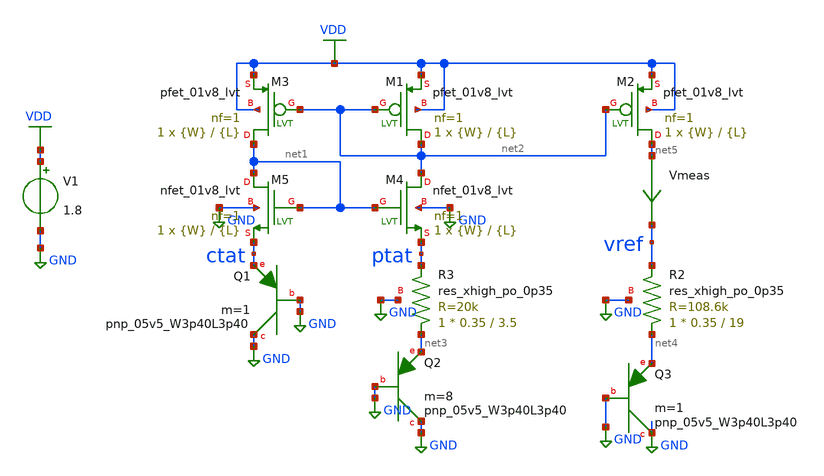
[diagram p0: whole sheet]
** sch_path: xschem/bgr.sch
**.subckt bgr
V1 VDD GND 1.8
XQ1 GND GND ctat sky130_fd_pr__pnp_05v5_W3p40L3p40 m=1
XQ2 GND GND net3 sky130_fd_pr__pnp_05v5_W3p40L3p40 m=8
XQ3 GND GND net4 sky130_fd_pr__pnp_05v5_W3p40L3p40 m=1
Vmeas net5 vref 0
.save i(vmeas)
XM3 net1 net2 VDD VDD sky130_fd_pr__pfet_01v8_lvt L={L} W={W} nf=1 ad='int((nf+1)/2) * W/nf * 0.29' as='int((nf+2)/2) * W/nf * 0.29'
+ pd='2*int((nf+1)/2) * (W/nf + 0.29)' ps='2*int((nf+2)/2) * (W/nf + 0.29)' nrd='0.29 / W' nrs='0.29 / W'
+ sa=0 sb=0 sd=0 mult=1 m=1
XM1 net2 net2 VDD VDD sky130_fd_pr__pfet_01v8_lvt L={L} W={W} nf=1 ad='int((nf+1)/2) * W/nf * 0.29' as='int((nf+2)/2) * W/nf * 0.29'
+ pd='2*int((nf+1)/2) * (W/nf + 0.29)' ps='2*int((nf+2)/2) * (W/nf + 0.29)' nrd='0.29 / W' nrs='0.29 / W'
+ sa=0 sb=0 sd=0 mult=1 m=1
XM2 net5 net2 VDD VDD sky130_fd_pr__pfet_01v8_lvt L={L} W={W} nf=1 ad='int((nf+1)/2) * W/nf * 0.29' as='int((nf+2)/2) * W/nf * 0.29'
+ pd='2*int((nf+1)/2) * (W/nf + 0.29)' ps='2*int((nf+2)/2) * (W/nf + 0.29)' nrd='0.29 / W' nrs='0.29 / W'
+ sa=0 sb=0 sd=0 mult=1 m=1
XM5 net1 net1 ctat GND sky130_fd_pr__nfet_01v8_lvt L={L} W={W} nf=1 ad='int((nf+1)/2) * W/nf * 0.29'
+ as='int((nf+2)/2) * W/nf * 0.29' pd='2*int((nf+1)/2) * (W/nf + 0.29)' ps='2*int((nf+2)/2) * (W/nf + 0.29)'
+ nrd='0.29 / W' nrs='0.29 / W' sa=0 sb=0 sd=0 mult=1 m=1
XM4 net2 net1 ptat GND sky130_fd_pr__nfet_01v8_lvt L={L} W={W} nf=1 ad='int((nf+1)/2) * W/nf * 0.29'
+ as='int((nf+2)/2) * W/nf * 0.29' pd='2*int((nf+1)/2) * (W/nf + 0.29)' ps='2*int((nf+2)/2) * (W/nf + 0.29)'
+ nrd='0.29 / W' nrs='0.29 / W' sa=0 sb=0 sd=0 mult=1 m=1
XR3 net3 ptat GND sky130_fd_pr__res_xhigh_po_0p35 L=3.5 mult=1 m=1
XR2 net4 vref GND sky130_fd_pr__res_xhigh_po_0p35 L=19 mult=1 m=1
**** begin user architecture code

** opencircuitdesign pdks install
.lib $::SKYWATER_MODELS/sky130.lib.spice tt




.param L=1.5
.param W=80




** Analysis Requests **
** Outputs Requests **
.option wnflag=1
.option savecurrents
.control
save all
dc temp -40 125 5
plot vref
op
save all
write bgr.raw
.endc


**** end user architecture code
**.ends
.GLOBAL VDD
.GLOBAL GND
.end
